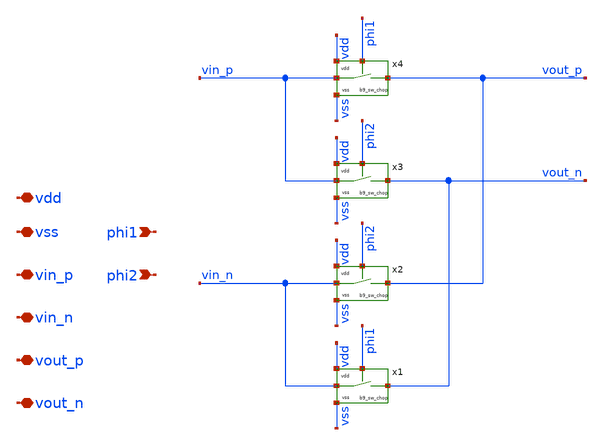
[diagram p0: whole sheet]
** sch_path: xschem/chopper/b9_chopper.sch
**.subckt b9_chopper vss vin_p vin_n vout_p vout_n phi1 phi2 vdd
*.iopin vss
*.iopin vin_p
*.iopin vin_n
*.iopin vout_p
*.iopin vout_n
*.ipin phi1
*.ipin phi2
*.iopin vdd
x1 vdd vin_n vss vout_n phi1 b9_sw_chop
x2 vdd vin_n vss vout_p phi2 b9_sw_chop
x3 vdd vin_p vss vout_n phi2 b9_sw_chop
x4 vdd vin_p vss vout_p phi1 b9_sw_chop
**.ends

* expanding   symbol:  xschem/sw/b9_sw_chop.sym # of pins=5
** sym_path: xschem/sw/b9_sw_chop.sym
** sch_path: xschem/sw/b9_sw_chop.sch
.subckt b9_sw_chop vdd va vss vb en
*.iopin vdd
*.iopin vss
*.iopin en
*.iopin va
*.iopin vb
XM1 vb en va vss nfet_03v3 L=0.28u W=3.2u nf=4 ad='int((nf+1)/2) * W/nf * 0.18u' as='int((nf+2)/2) * W/nf * 0.18u'
+ pd='2*int((nf+1)/2) * (W/nf + 0.18u)' ps='2*int((nf+2)/2) * (W/nf + 0.18u)' nrd='0.18u / W' nrs='0.18u / W'
+ sa=0 sb=0 sd=0 m=1
.ends

.end
